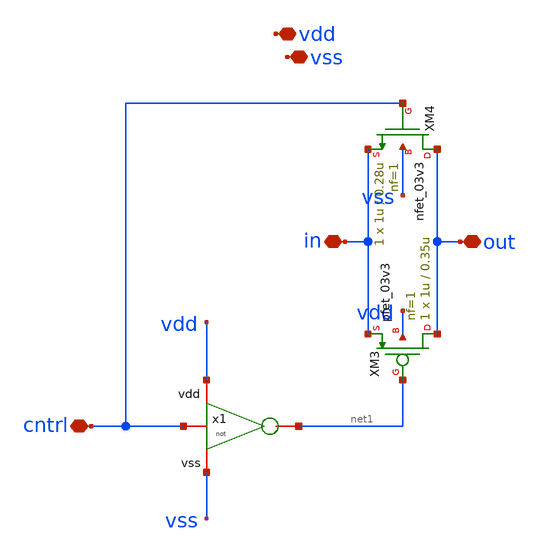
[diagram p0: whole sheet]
** sch_path: designs/libs/core_LIF_comp/core_switch/switch.sch
**.subckt switch vdd vss in out cntrl
*.iopin vdd
*.iopin vss
*.iopin in
*.iopin out
*.iopin cntrl
x1 vdd cntrl net1 vss not
XM3 out net1 in vdd pfet_03v3 L=0.35u W=1u nf=1 ad='int((nf+1)/2) * W/nf * 0.18u' as='int((nf+2)/2) * W/nf * 0.18u'
+ pd='2*int((nf+1)/2) * (W/nf + 0.18u)' ps='2*int((nf+2)/2) * (W/nf + 0.18u)' nrd='0.18u / W' nrs='0.18u / W'
+ sa=0 sb=0 sd=0 m=1
XM4 out cntrl in vss nfet_03v3 L=0.28u W=1u nf=1 ad='int((nf+1)/2) * W/nf * 0.18u' as='int((nf+2)/2) * W/nf * 0.18u'
+ pd='2*int((nf+1)/2) * (W/nf + 0.18u)' ps='2*int((nf+2)/2) * (W/nf + 0.18u)' nrd='0.18u / W' nrs='0.18u / W'
+ sa=0 sb=0 sd=0 m=1
**.ends

* expanding   symbol:  designs/libs/core_LIF_comp/core_not/not.sym # of pins=4
** sym_path: designs/libs/core_LIF_comp/core_not/not.sym
** sch_path: designs/libs/core_LIF_comp/core_not/not.sch
.subckt not vdd in out vss
*.iopin vdd
*.iopin vss
*.iopin in
*.iopin out
XM1 out in vdd vdd pfet_03v3 L=0.35u W=1u nf=1 ad='int((nf+1)/2) * W/nf * 0.18u' as='int((nf+2)/2) * W/nf * 0.18u'
+ pd='2*int((nf+1)/2) * (W/nf + 0.18u)' ps='2*int((nf+2)/2) * (W/nf + 0.18u)' nrd='0.18u / W' nrs='0.18u / W'
+ sa=0 sb=0 sd=0 m=1
XM3 out in vss vss nfet_03v3 L=0.28u W=1u nf=1 ad='int((nf+1)/2) * W/nf * 0.18u' as='int((nf+2)/2) * W/nf * 0.18u'
+ pd='2*int((nf+1)/2) * (W/nf + 0.18u)' ps='2*int((nf+2)/2) * (W/nf + 0.18u)' nrd='0.18u / W' nrs='0.18u / W'
+ sa=0 sb=0 sd=0 m=1
.ends

.end
